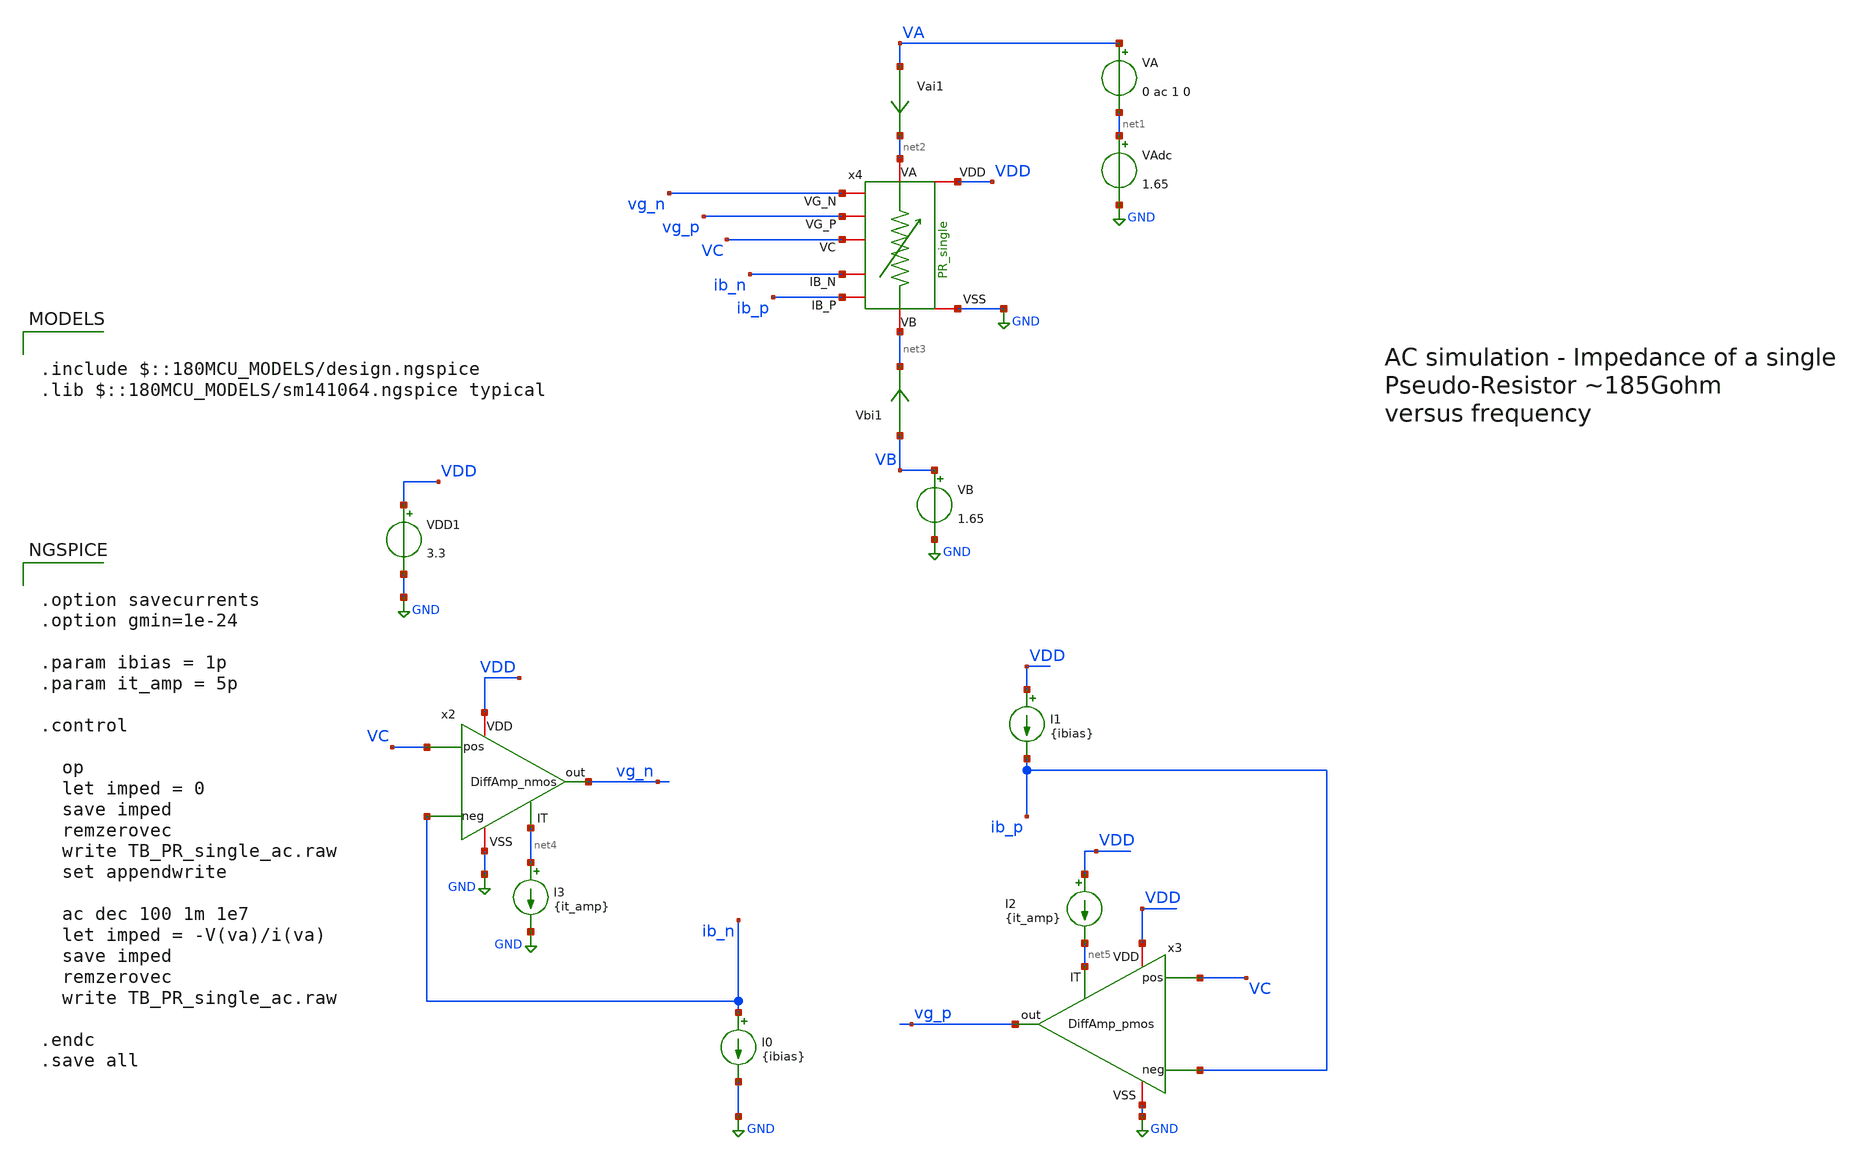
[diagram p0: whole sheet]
** sch_path: TIA/xschem/PseudoResistor/TB_PR_single_ac.sch
**.subckt TB_PR_single_ac
VDD1 VDD GND 3.3
VA VA net1 0 ac 1 0
VB VB GND 1.65
VAdc net1 GND 1.65
Vai1 VA net2 0
.save i(vai1)
Vbi1 VB net3 0
.save i(vbi1)
x4 net2 net3 vg_n vg_p ib_n ib_p VDD GND VC PR_single
I0 ib_n GND {ibias}
I1 VDD ib_p {ibias}
x2 VDD GND VC ib_n net4 vg_n DiffAmp_nmos
I2 VDD net5 {it_amp}
x3 VDD GND net5 ib_p VC vg_p DiffAmp_pmos
I3 net4 GND {it_amp}
**** begin user architecture code

.include $::180MCU_MODELS/design.ngspice
.lib $::180MCU_MODELS/sm141064.ngspice typical



.option savecurrents
.option gmin=1e-24

.param ibias = 1p
.param it_amp = 5p

.control

  op
  let imped = 0
  save imped
  remzerovec
  write TB_PR_single_ac.raw
  set appendwrite

  ac dec 100 1m 1e7
  let imped = -V(va)/i(va)
  save imped
  remzerovec
  write TB_PR_single_ac.raw

.endc
.save all


**** end user architecture code
**.ends
.GLOBAL GND
.end
